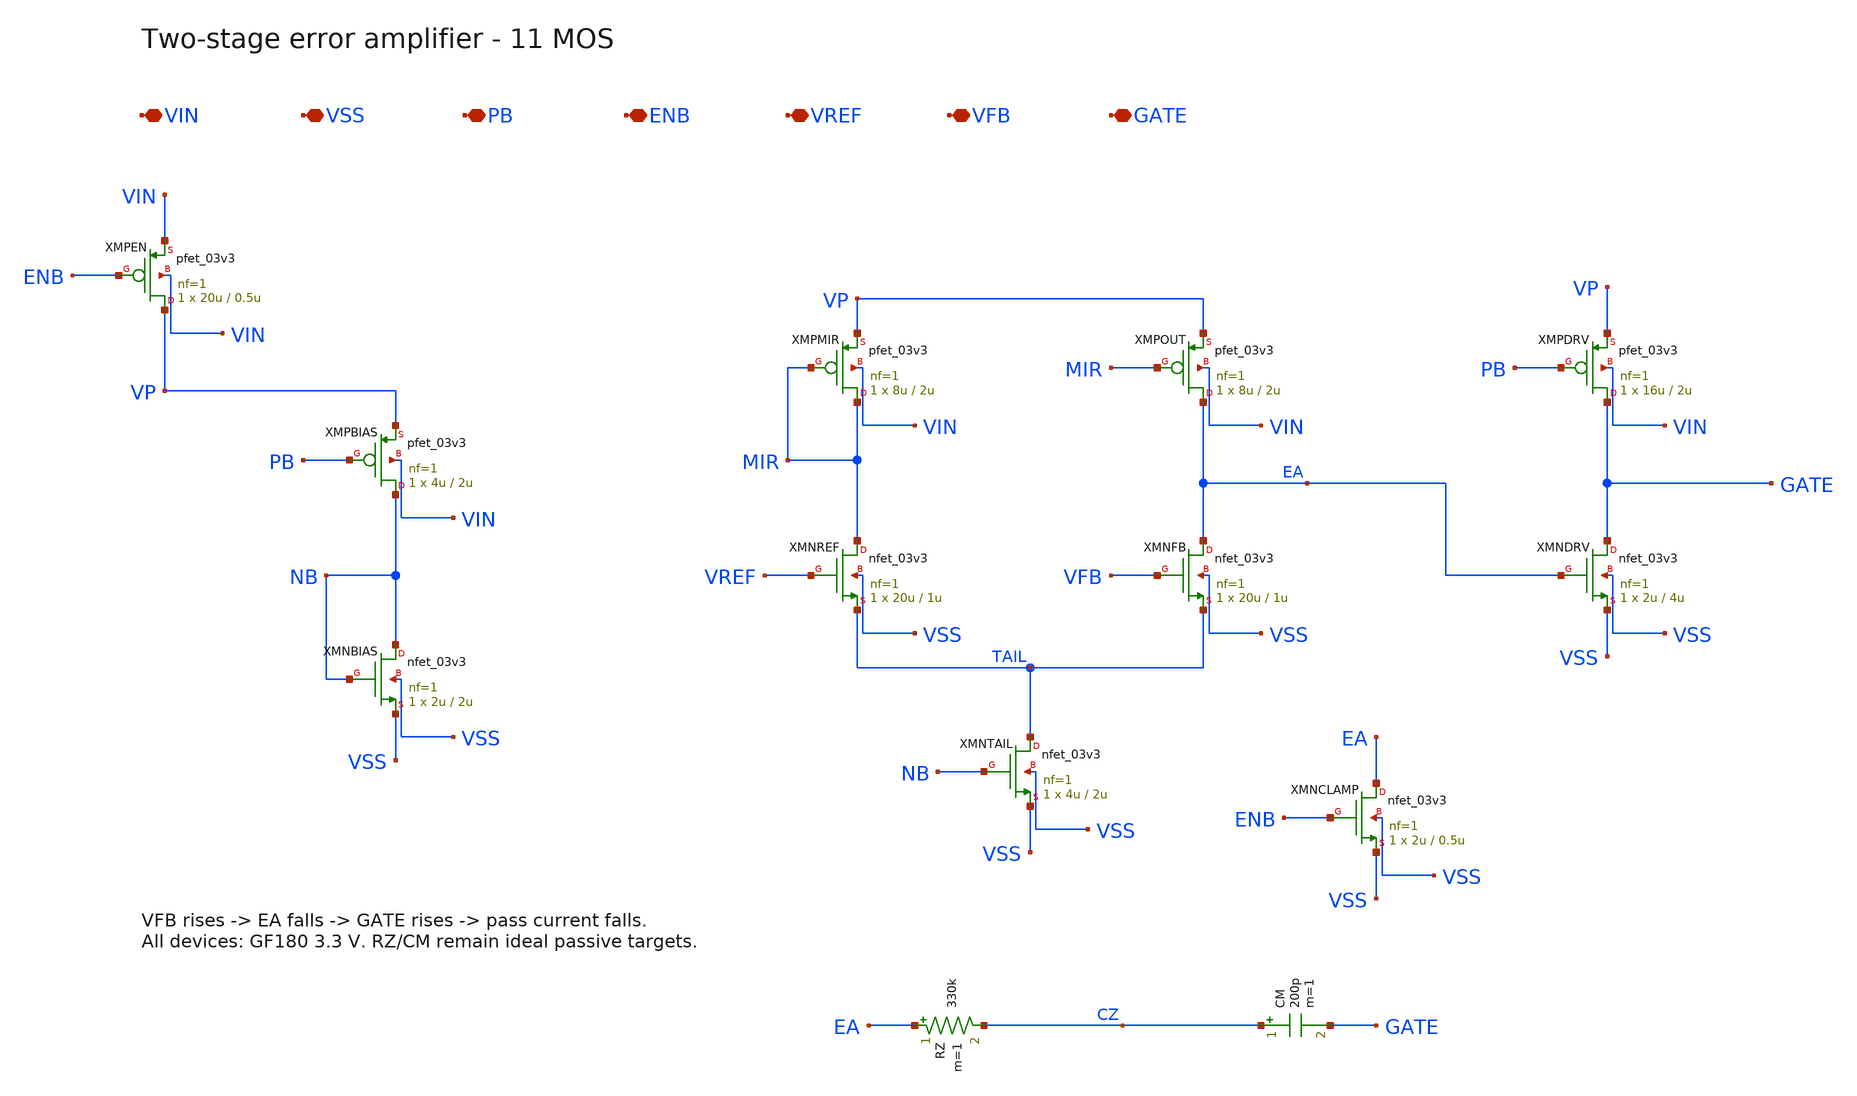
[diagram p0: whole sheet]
** sch_path: schematics/ldo_error_amp.sch
**.subckt ldo_error_amp VIN VSS PB ENB VREF VFB GATE
*.iopin VIN
*.iopin VSS
*.iopin PB
*.iopin ENB
*.iopin VREF
*.iopin VFB
*.iopin GATE
XMPEN VP ENB VIN VIN pfet_03v3 L=0.5u W=20u nf=1 ad='int((nf+1)/2)*W/nf*0.18u' as='int((nf+2)/2)*W/nf*0.18u'
+ pd='2*int((nf+1)/2)*(W/nf+0.18u)' ps='2*int((nf+2)/2)*(W/nf+0.18u)' nrd='0.18u/W' nrs='0.18u/W' sa=0
+ sb=0 sd=0 m=1 par=1
XMPBIAS NB PB VP VIN pfet_03v3 L=2u W=4u nf=1 ad='int((nf+1)/2)*W/nf*0.18u' as='int((nf+2)/2)*W/nf*0.18u'
+ pd='2*int((nf+1)/2)*(W/nf+0.18u)' ps='2*int((nf+2)/2)*(W/nf+0.18u)' nrd='0.18u/W' nrs='0.18u/W' sa=0
+ sb=0 sd=0 m=1 par=1
XMNBIAS NB NB VSS VSS nfet_03v3 L=2u W=2u nf=1 ad='int((nf+1)/2)*W/nf*0.18u' as='int((nf+2)/2)*W/nf*0.18u'
+ pd='2*int((nf+1)/2)*(W/nf+0.18u)' ps='2*int((nf+2)/2)*(W/nf+0.18u)' nrd='0.18u/W' nrs='0.18u/W' sa=0
+ sb=0 sd=0 m=1 par=1
XMPMIR MIR MIR VP VIN pfet_03v3 L=2u W=8u nf=1 ad='int((nf+1)/2)*W/nf*0.18u' as='int((nf+2)/2)*W/nf*0.18u'
+ pd='2*int((nf+1)/2)*(W/nf+0.18u)' ps='2*int((nf+2)/2)*(W/nf+0.18u)' nrd='0.18u/W' nrs='0.18u/W' sa=0
+ sb=0 sd=0 m=1 par=1
XMPOUT EA MIR VP VIN pfet_03v3 L=2u W=8u nf=1 ad='int((nf+1)/2)*W/nf*0.18u' as='int((nf+2)/2)*W/nf*0.18u'
+ pd='2*int((nf+1)/2)*(W/nf+0.18u)' ps='2*int((nf+2)/2)*(W/nf+0.18u)' nrd='0.18u/W' nrs='0.18u/W' sa=0
+ sb=0 sd=0 m=1 par=1
XMNREF MIR VREF TAIL VSS nfet_03v3 L=1u W=20u nf=1 ad='int((nf+1)/2)*W/nf*0.18u' as='int((nf+2)/2)*W/nf*0.18u'
+ pd='2*int((nf+1)/2)*(W/nf+0.18u)' ps='2*int((nf+2)/2)*(W/nf+0.18u)' nrd='0.18u/W' nrs='0.18u/W' sa=0
+ sb=0 sd=0 m=1 par=1
XMNFB EA VFB TAIL VSS nfet_03v3 L=1u W=20u nf=1 ad='int((nf+1)/2)*W/nf*0.18u' as='int((nf+2)/2)*W/nf*0.18u'
+ pd='2*int((nf+1)/2)*(W/nf+0.18u)' ps='2*int((nf+2)/2)*(W/nf+0.18u)' nrd='0.18u/W' nrs='0.18u/W' sa=0
+ sb=0 sd=0 m=1 par=1
XMNTAIL TAIL NB VSS VSS nfet_03v3 L=2u W=4u nf=1 ad='int((nf+1)/2)*W/nf*0.18u' as='int((nf+2)/2)*W/nf*0.18u'
+ pd='2*int((nf+1)/2)*(W/nf+0.18u)' ps='2*int((nf+2)/2)*(W/nf+0.18u)' nrd='0.18u/W' nrs='0.18u/W' sa=0
+ sb=0 sd=0 m=1 par=1
XMPDRV GATE PB VP VIN pfet_03v3 L=2u W=16u nf=1 ad='int((nf+1)/2)*W/nf*0.18u' as='int((nf+2)/2)*W/nf*0.18u'
+ pd='2*int((nf+1)/2)*(W/nf+0.18u)' ps='2*int((nf+2)/2)*(W/nf+0.18u)' nrd='0.18u/W' nrs='0.18u/W' sa=0
+ sb=0 sd=0 m=1 par=1
XMNDRV GATE EA VSS VSS nfet_03v3 L=4u W=2u nf=1 ad='int((nf+1)/2)*W/nf*0.18u' as='int((nf+2)/2)*W/nf*0.18u'
+ pd='2*int((nf+1)/2)*(W/nf+0.18u)' ps='2*int((nf+2)/2)*(W/nf+0.18u)' nrd='0.18u/W' nrs='0.18u/W' sa=0
+ sb=0 sd=0 m=1 par=1
XMNCLAMP EA ENB VSS VSS nfet_03v3 L=0.5u W=2u nf=1 ad='int((nf+1)/2)*W/nf*0.18u' as='int((nf+2)/2)*W/nf*0.18u'
+ pd='2*int((nf+1)/2)*(W/nf+0.18u)' ps='2*int((nf+2)/2)*(W/nf+0.18u)' nrd='0.18u/W' nrs='0.18u/W' sa=0
+ sb=0 sd=0 m=1 par=1
RZ EA CZ 330k m=1
CM CZ GATE 200p m=1
**.ends
.end
